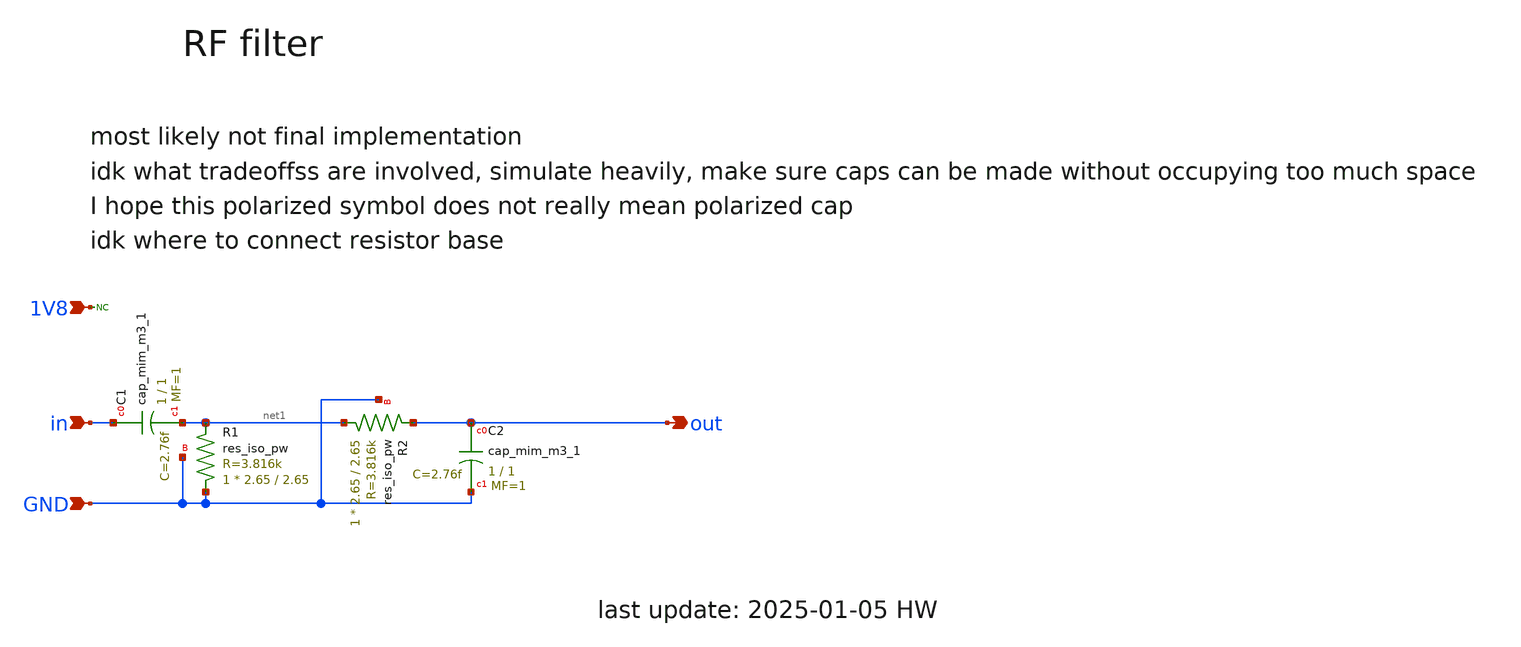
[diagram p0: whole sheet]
** sch_path: schematic/rf_filter.sch
**.subckt rf_filter in out GND 1V8
*.ipin in
*.opin out
*.ipin GND
*.ipin 1V8
* noconn 1V8
XR1 GND net1 GND sky130_fd_pr__res_iso_pw W=2.65 L=2.65 m=1
XC1 in net1 sky130_fd_pr__cap_mim_m3_1 W=1 L=1 MF=1 m=1
XR2 net1 out GND sky130_fd_pr__res_iso_pw W=2.65 L=2.65 m=1
XC2 out GND sky130_fd_pr__cap_mim_m3_1 W=1 L=1 MF=1 m=1
**.ends
.end
